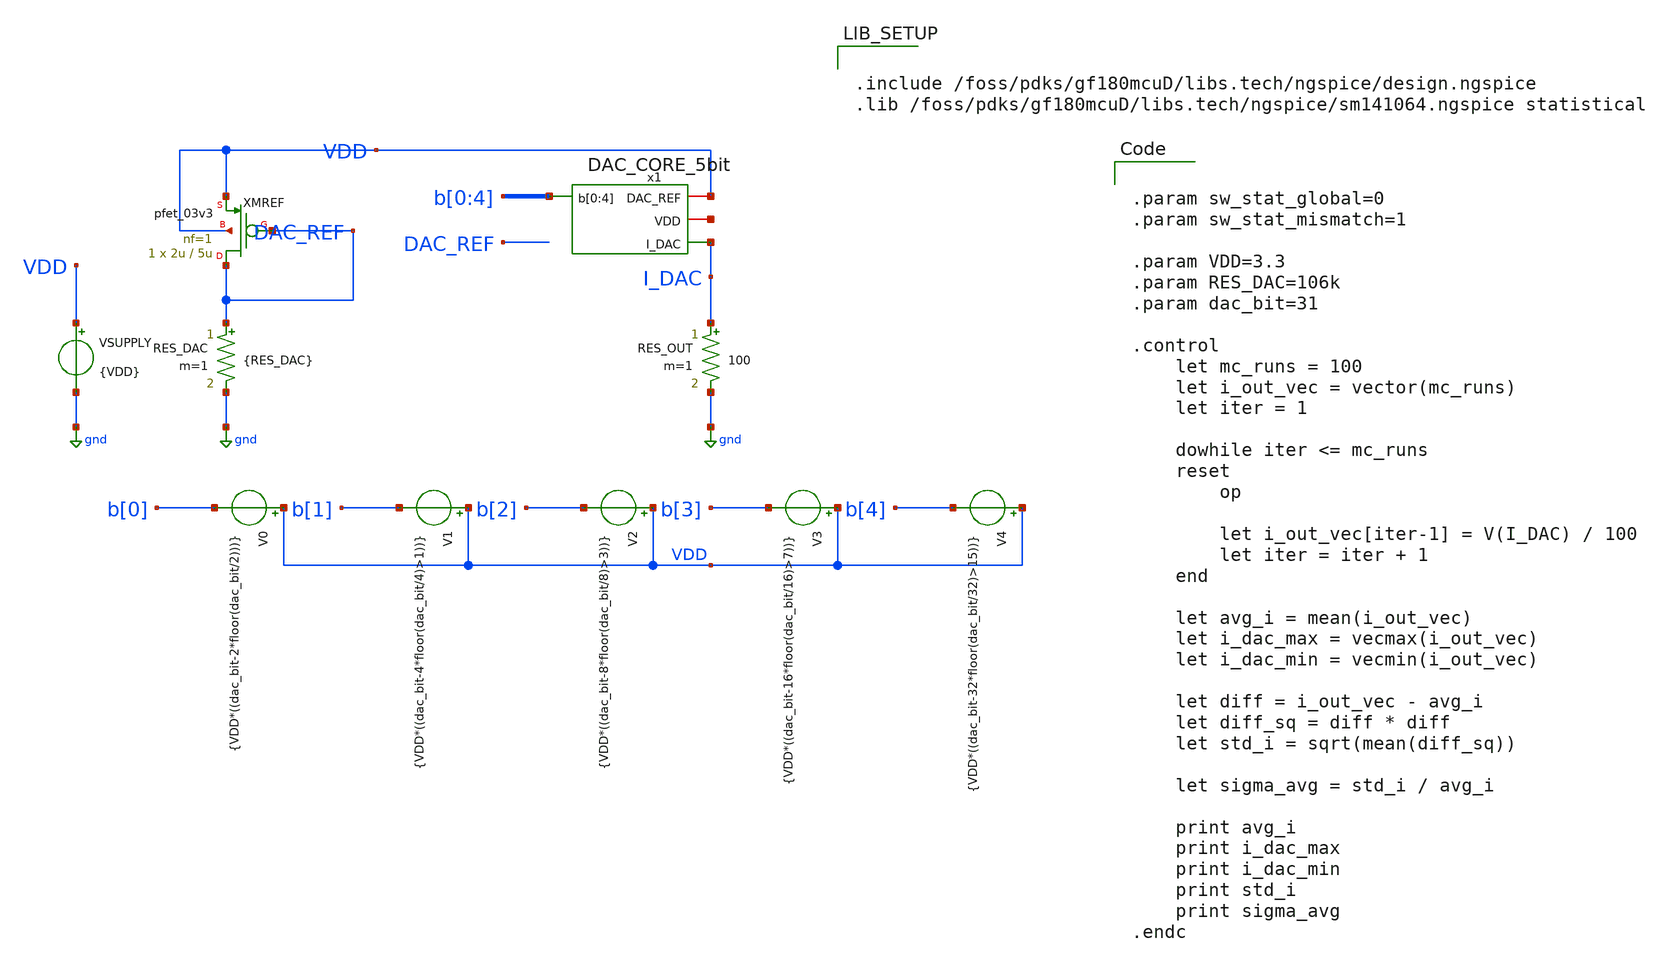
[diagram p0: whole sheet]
** sch_path: DAC_CORE_5bit/DAC_CORE_5bit_test.sch
**.subckt DAC_CORE_5bit_test
XMREF DAC_REF DAC_REF VDD VDD pfet_03v3 L=5u W=2u nf=1 ad='int((nf+1)/2) * W/nf * 0.18u' as='int((nf+2)/2) * W/nf * 0.18u'
+ pd='2*int((nf+1)/2) * (W/nf + 0.18u)' ps='2*int((nf+2)/2) * (W/nf + 0.18u)' nrd='0.18u / W' nrs='0.18u / W'
+ sa=0 sb=0 sd=0 m=1
RES_DAC DAC_REF gnd {RES_DAC} m=1
RES_OUT I_DAC gnd 100 m=1
V0 VDD b[0] {VDD*((dac_bit-2*floor(dac_bit/2)))}
VSUPPLY VDD gnd {VDD}
V1 VDD b[1] {VDD*((dac_bit-4*floor(dac_bit/4)>1))}
V2 VDD b[2] {VDD*((dac_bit-8*floor(dac_bit/8)>3))}
V3 VDD b[3] {VDD*((dac_bit-16*floor(dac_bit/16)>7))}
V4 VDD b[4] {VDD*((dac_bit-32*floor(dac_bit/32)>15))}
x1 VDD net1 b[0] b[1] b[2] b[3] b[4] I_DAC DAC_CORE_5bit
**** begin user architecture code


.include /foss/pdks/gf180mcuD/libs.tech/ngspice/design.ngspice
.lib /foss/pdks/gf180mcuD/libs.tech/ngspice/sm141064.ngspice statistical




.param sw_stat_global=0
.param sw_stat_mismatch=1

.param VDD=3.3
.param RES_DAC=106k
.param dac_bit=31

.control
    let mc_runs = 100
    let i_out_vec = vector(mc_runs)
    let iter = 1

    dowhile iter <= mc_runs
	reset
        op

        let i_out_vec[iter-1] = V(I_DAC) / 100
        let iter = iter + 1
    end

    let avg_i = mean(i_out_vec)
    let i_dac_max = vecmax(i_out_vec)
    let i_dac_min = vecmin(i_out_vec)

    let diff = i_out_vec - avg_i
    let diff_sq = diff * diff
    let std_i = sqrt(mean(diff_sq))

    let sigma_avg = std_i / avg_i

    print avg_i
    print i_dac_max
    print i_dac_min
    print std_i
    print sigma_avg
.endc


**** end user architecture code
**.ends

* expanding   symbol:  DAC_CORE_5bit/DAC_CORE_5bit.sym # of pins=4
** sym_path: DAC_CORE_5bit/DAC_CORE_5bit.sym
** sch_path: DAC_CORE_5bit/DAC_CORE_5bit.sch
.subckt DAC_CORE_5bit DAC_REF VDD b[0] b[1] b[2] b[3] b[4] I_DAC
*.opin I_DAC
*.iopin VDD
*.iopin DAC_REF
*.ipin b[0],b[1],b[2],b[3],b[4]
XMK1 I_DAC b[0] net5 VDD pfet_03v3 L=0.28u W=0.78u nf=1 ad='int((nf+1)/2) * W/nf * 0.18u' as='int((nf+2)/2) * W/nf * 0.18u'
+ pd='2*int((nf+1)/2) * (W/nf + 0.18u)' ps='2*int((nf+2)/2) * (W/nf + 0.18u)' nrd='0.18u / W' nrs='0.18u / W'
+ sa=0 sb=0 sd=0 m=1
XMK2 I_DAC b[1] net1 VDD pfet_03v3 L=0.28u W=0.78u nf=1 ad='int((nf+1)/2) * W/nf * 0.18u' as='int((nf+2)/2) * W/nf * 0.18u'
+ pd='2*int((nf+1)/2) * (W/nf + 0.18u)' ps='2*int((nf+2)/2) * (W/nf + 0.18u)' nrd='0.18u / W' nrs='0.18u / W'
+ sa=0 sb=0 sd=0 m=2
XMK3 I_DAC b[2] net2 VDD pfet_03v3 L=0.28u W=0.78u nf=1 ad='int((nf+1)/2) * W/nf * 0.18u' as='int((nf+2)/2) * W/nf * 0.18u'
+ pd='2*int((nf+1)/2) * (W/nf + 0.18u)' ps='2*int((nf+2)/2) * (W/nf + 0.18u)' nrd='0.18u / W' nrs='0.18u / W'
+ sa=0 sb=0 sd=0 m=4
XMK4 I_DAC b[3] net3 VDD pfet_03v3 L=0.28u W=0.78u nf=1 ad='int((nf+1)/2) * W/nf * 0.18u' as='int((nf+2)/2) * W/nf * 0.18u'
+ pd='2*int((nf+1)/2) * (W/nf + 0.18u)' ps='2*int((nf+2)/2) * (W/nf + 0.18u)' nrd='0.18u / W' nrs='0.18u / W'
+ sa=0 sb=0 sd=0 m=8
XMK5 I_DAC b[4] net4 VDD pfet_03v3 L=0.28u W=0.78u nf=1 ad='int((nf+1)/2) * W/nf * 0.18u' as='int((nf+2)/2) * W/nf * 0.18u'
+ pd='2*int((nf+1)/2) * (W/nf + 0.18u)' ps='2*int((nf+2)/2) * (W/nf + 0.18u)' nrd='0.18u / W' nrs='0.18u / W'
+ sa=0 sb=0 sd=0 m=16
XM1 net5 DAC_REF VDD VDD pfet_03v3 L=2u W=5u nf=1 ad='int((nf+1)/2) * W/nf * 0.18u' as='int((nf+2)/2) * W/nf * 0.18u'
+ pd='2*int((nf+1)/2) * (W/nf + 0.18u)' ps='2*int((nf+2)/2) * (W/nf + 0.18u)' nrd='0.18u / W' nrs='0.18u / W'
+ sa=0 sb=0 sd=0 m=1
XM2 net1 DAC_REF VDD VDD pfet_03v3 L=2u W=5u nf=1 ad='int((nf+1)/2) * W/nf * 0.18u' as='int((nf+2)/2) * W/nf * 0.18u'
+ pd='2*int((nf+1)/2) * (W/nf + 0.18u)' ps='2*int((nf+2)/2) * (W/nf + 0.18u)' nrd='0.18u / W' nrs='0.18u / W'
+ sa=0 sb=0 sd=0 m=2
XM3 net2 DAC_REF VDD VDD pfet_03v3 L=2u W=5u nf=1 ad='int((nf+1)/2) * W/nf * 0.18u' as='int((nf+2)/2) * W/nf * 0.18u'
+ pd='2*int((nf+1)/2) * (W/nf + 0.18u)' ps='2*int((nf+2)/2) * (W/nf + 0.18u)' nrd='0.18u / W' nrs='0.18u / W'
+ sa=0 sb=0 sd=0 m=4
XM4 net3 DAC_REF VDD VDD pfet_03v3 L=2u W=5u nf=1 ad='int((nf+1)/2) * W/nf * 0.18u' as='int((nf+2)/2) * W/nf * 0.18u'
+ pd='2*int((nf+1)/2) * (W/nf + 0.18u)' ps='2*int((nf+2)/2) * (W/nf + 0.18u)' nrd='0.18u / W' nrs='0.18u / W'
+ sa=0 sb=0 sd=0 m=8
XM5 net4 DAC_REF VDD VDD pfet_03v3 L=2u W=5u nf=1 ad='int((nf+1)/2) * W/nf * 0.18u' as='int((nf+2)/2) * W/nf * 0.18u'
+ pd='2*int((nf+1)/2) * (W/nf + 0.18u)' ps='2*int((nf+2)/2) * (W/nf + 0.18u)' nrd='0.18u / W' nrs='0.18u / W'
+ sa=0 sb=0 sd=0 m=16
.ends

.GLOBAL gnd
.end
